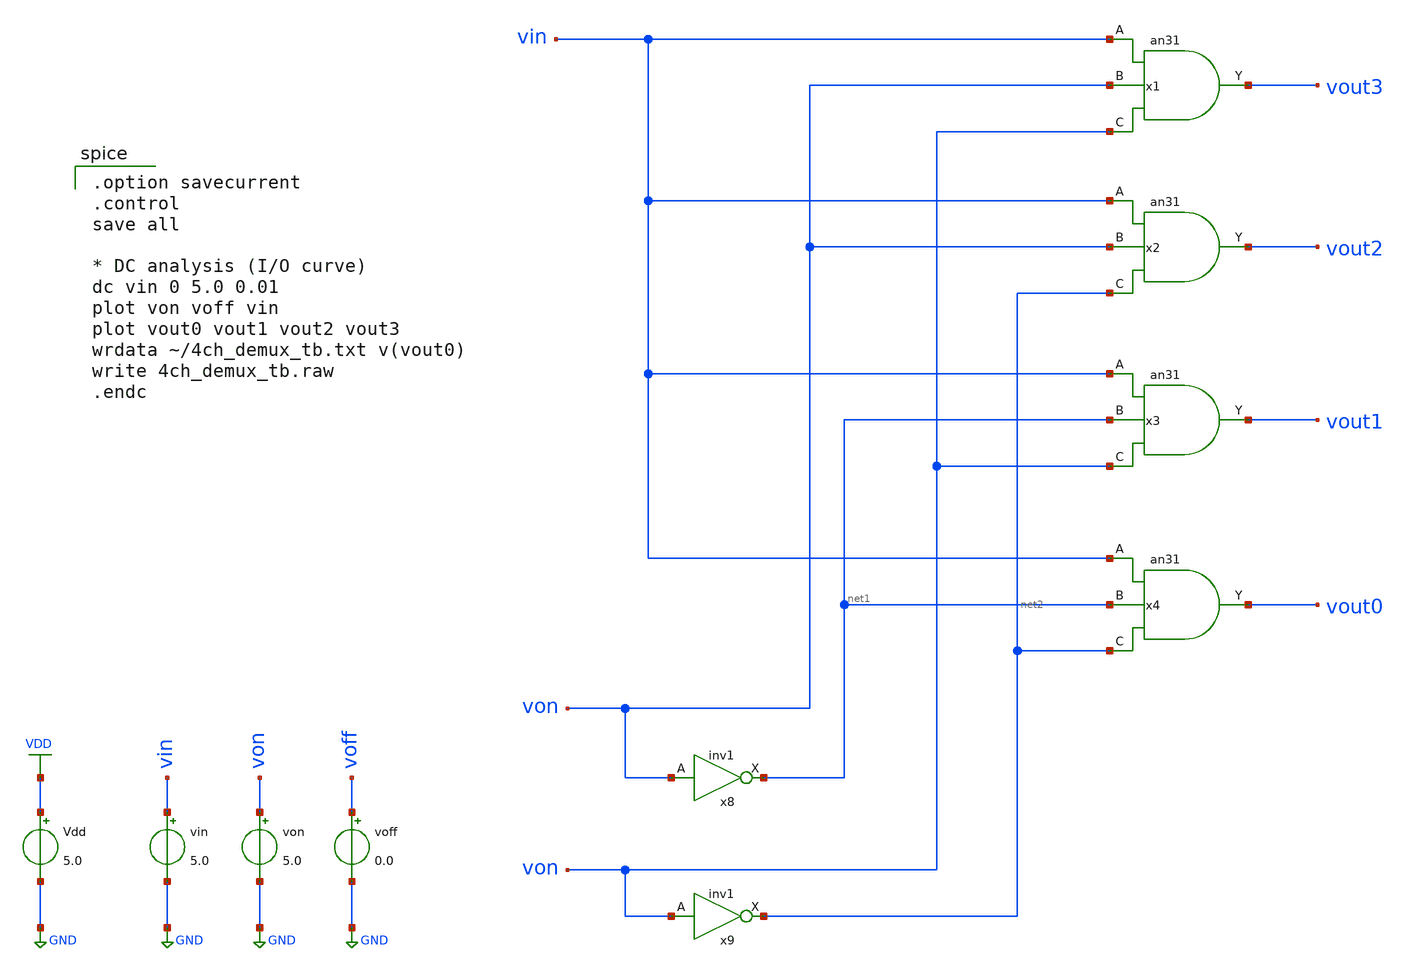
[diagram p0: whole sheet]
** sch_path: member_project/ishi-kai/4ch_demux_tb.sch
**.subckt 4ch_demux_tb
x1 vin von von VDD GND vout3 an31
x2 vin von net2 VDD GND vout2 an31
x3 vin net1 von VDD GND vout1 an31
x4 vin net1 net2 VDD GND vout0 an31
x8 von VDD GND net1 inv1
x9 von VDD GND net2 inv1
Vdd VDD GND 5.0
von von GND 5.0
voff voff GND 0.0
vin vin GND 5.0
**** begin user architecture code
 .include $::LIB/mos.lib
.include $::LIB/passive.lib
.include $::LIB/diode.lib

.option savecurrent
.control
save all

* DC analysis (I/O curve)
dc vin 0 5.0 0.01
plot von voff vin
plot vout0 vout1 vout2 vout3
wrdata ~/4ch_demux_tb.txt v(vout0)
write 4ch_demux_tb.raw
.endc

**** end user architecture code
**.ends
.GLOBAL VDD
.GLOBAL GND
.end
